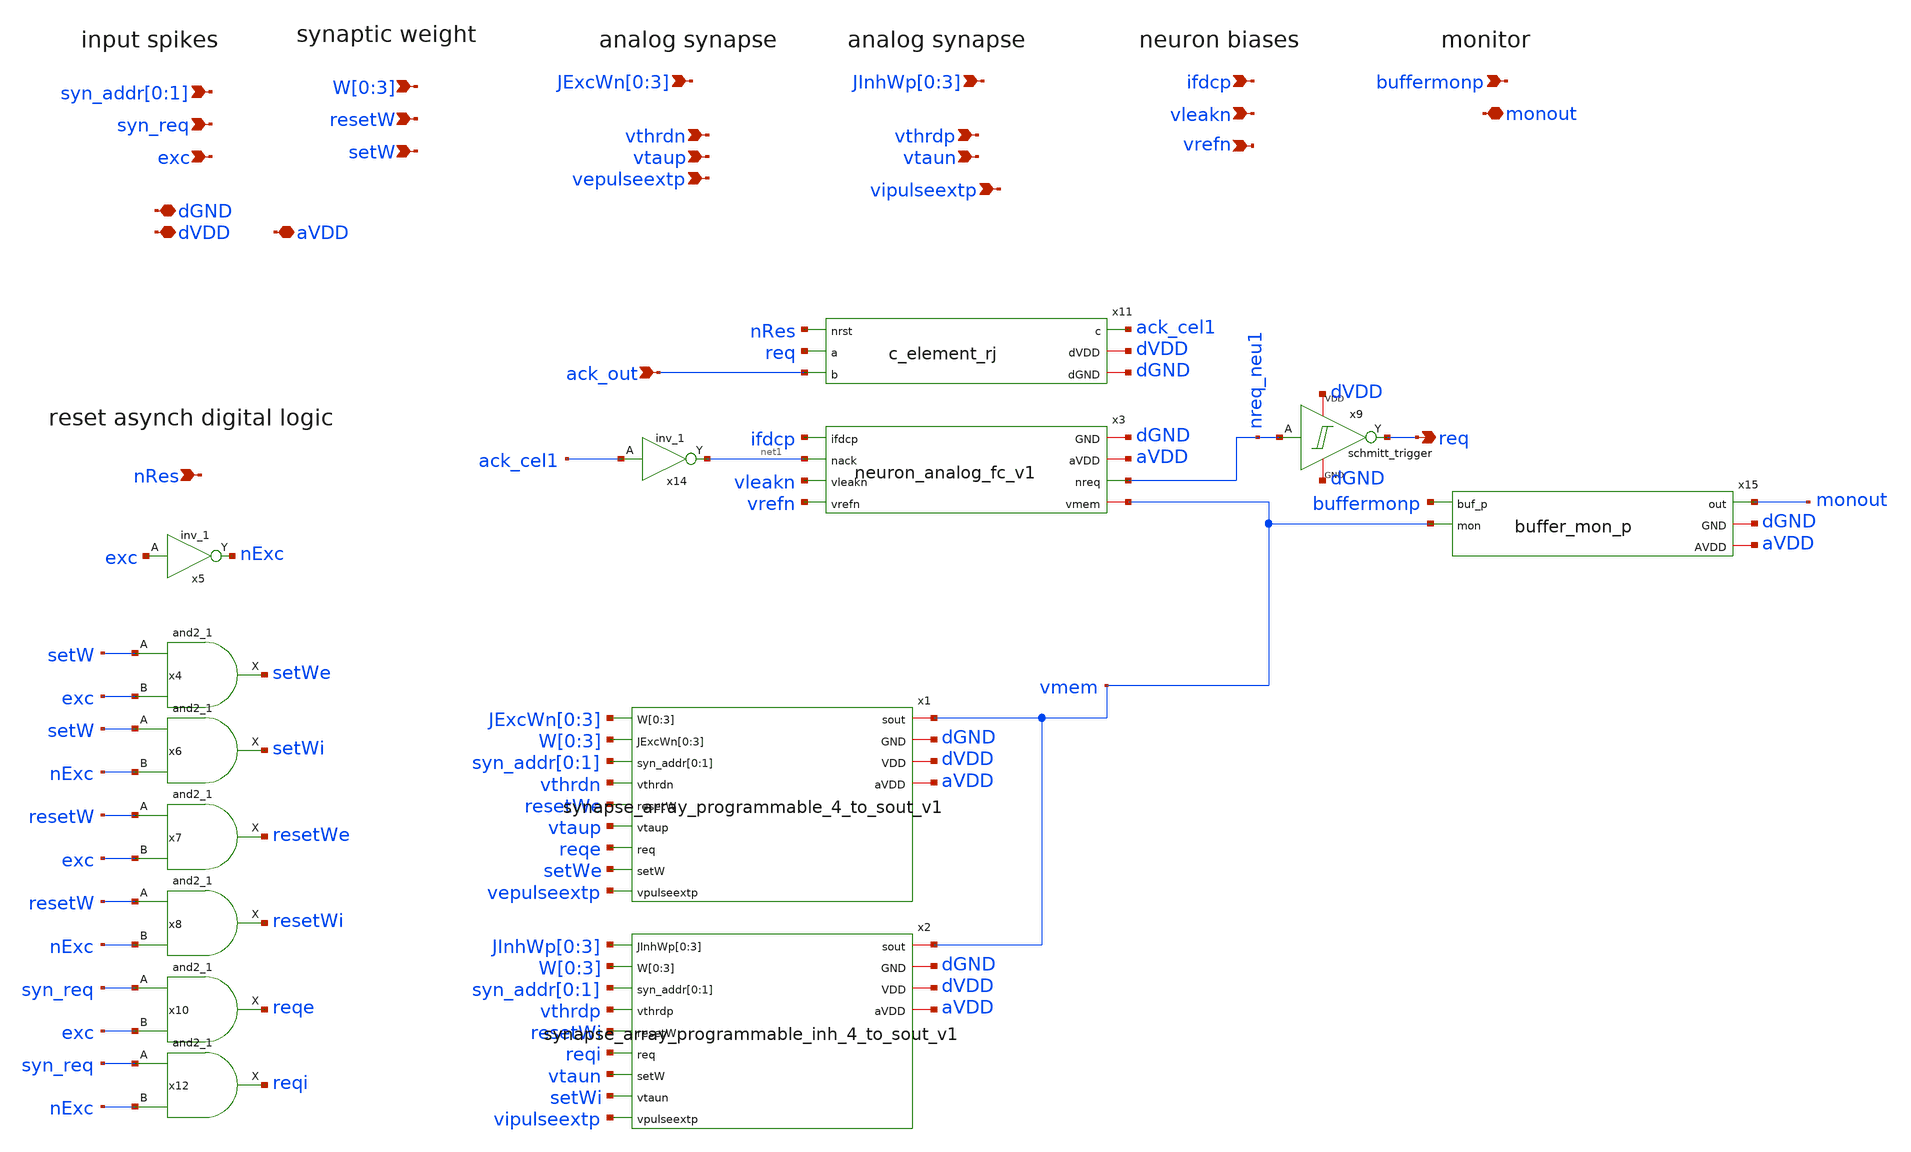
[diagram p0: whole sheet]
** sch_path: design/xschem/neuron_4syn_v1.sch
**.subckt neuron_4syn_v1 ack_out dGND dVDD vepulseextp syn_addr[0],syn_addr[1] W[0],W[1],W[2],W[3]
*+ setW resetW syn_req exc vipulseextp req vleakn ifdcp vrefn nRes aVDD buffermonp monout
*+ JExcWn[0],JExcWn[1],JExcWn[2],JExcWn[3] JInhWp[0],JInhWp[1],JInhWp[2],JInhWp[3] vtaup vthrdn vtaun vthrdp
*.ipin ack_out
*.iopin dGND
*.iopin dVDD
*.ipin vepulseextp
*.ipin syn_addr[0],syn_addr[1]
*.ipin W[0],W[1],W[2],W[3]
*.ipin setW
*.ipin resetW
*.ipin syn_req
*.ipin exc
*.ipin vipulseextp
*.opin req
*.ipin vleakn
*.ipin ifdcp
*.ipin vrefn
*.ipin nRes
*.iopin aVDD
*.ipin buffermonp
*.iopin monout
*.ipin JExcWn[0],JExcWn[1],JExcWn[2],JExcWn[3]
*.ipin JInhWp[0],JInhWp[1],JInhWp[2],JInhWp[3]
*.ipin vtaup
*.ipin vthrdn
*.ipin vtaun
*.ipin vthrdp
x11 nRes req ack_out ack_cel1 dVDD dGND c_element_rj
x4 setW exc dGND dGND dVDD dVDD setWe sky130_fd_sc_hd__and2_1
x5 exc dGND dGND dVDD dVDD nExc sky130_fd_sc_hd__inv_1
x6 setW nExc dGND dGND dVDD dVDD setWi sky130_fd_sc_hd__and2_1
x7 resetW exc dGND dGND dVDD dVDD resetWe sky130_fd_sc_hd__and2_1
x8 resetW nExc dGND dGND dVDD dVDD resetWi sky130_fd_sc_hd__and2_1
x10 syn_req exc dGND dGND dVDD dVDD reqe sky130_fd_sc_hd__and2_1
x12 syn_req nExc dGND dGND dVDD dVDD reqi sky130_fd_sc_hd__and2_1
x14 ack_cel1 dGND dGND dVDD dVDD net1 sky130_fd_sc_hd__inv_1
x3 dGND aVDD nreq_neu1 ifdcp net1 vmem vleakn vrefn neuron_analog_fc_v1
x1 JExcWn[0] JExcWn[1] JExcWn[2] JExcWn[3] W[0] W[1] W[2] W[3] vmem syn_addr[0] syn_addr[1] vthrdn
+ resetWe vtaup reqe setWe vepulseextp dGND dVDD aVDD synapse_array_programmable_4_to_sout_v1
x2 vmem JInhWp[0] JInhWp[1] JInhWp[2] JInhWp[3] W[0] W[1] W[2] W[3] syn_addr[0] syn_addr[1] vthrdp
+ resetWi reqi vtaun setWi vipulseextp dGND dVDD aVDD synapse_array_programmable_inh_4_to_sout_v1
x15 buffermonp monout vmem dGND aVDD buffer_mon_p
x9 nreq_neu1 req dVDD dGND schmitt_trigger
**.ends
.end
